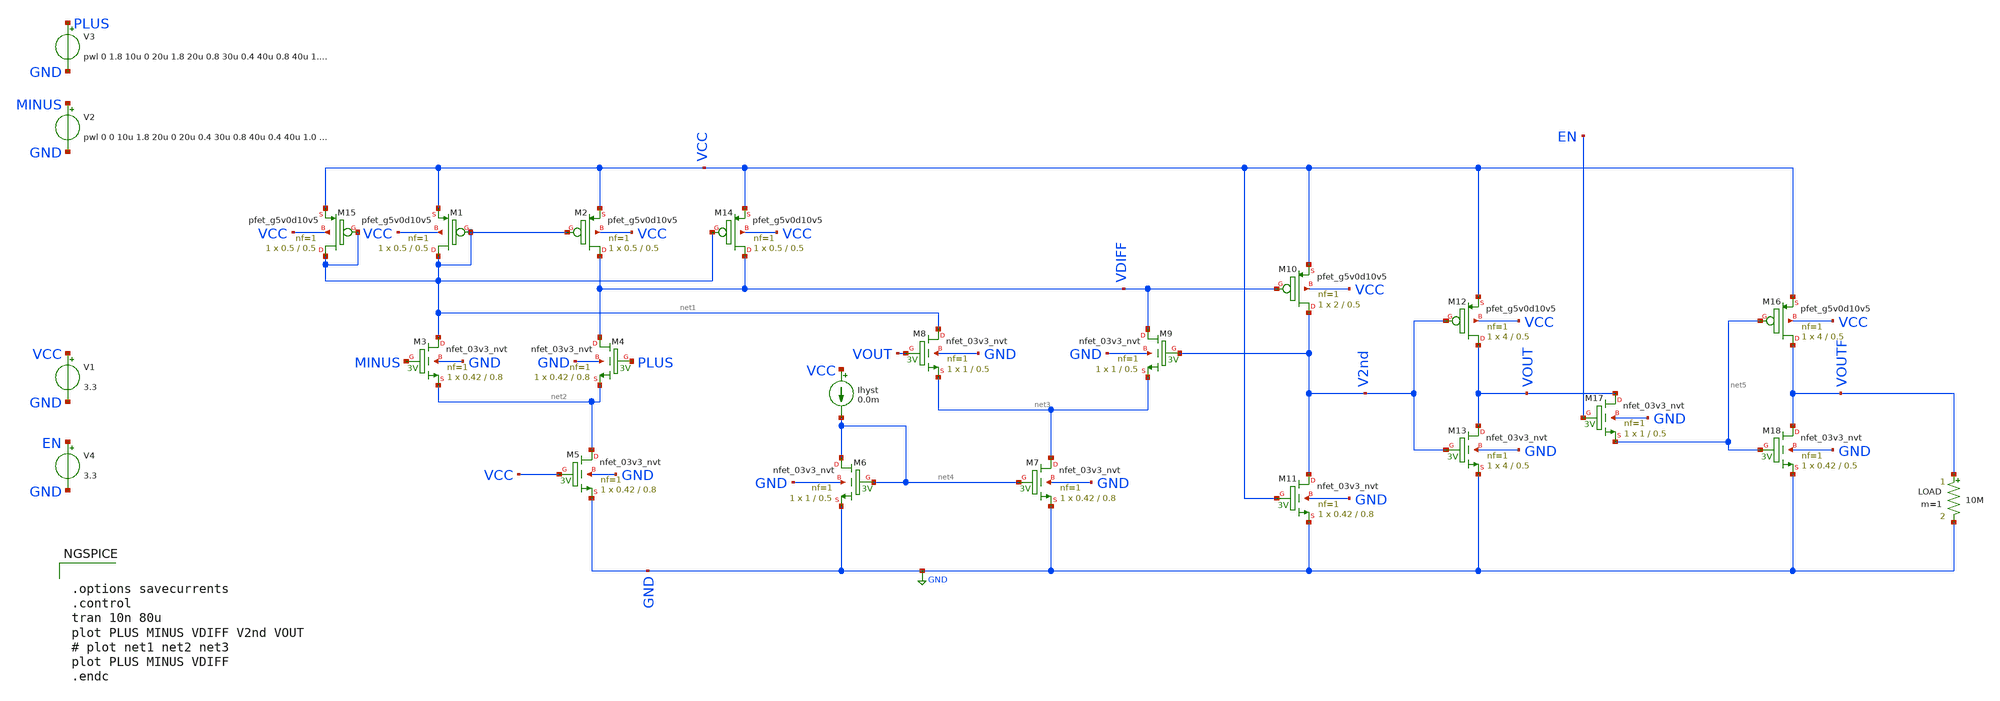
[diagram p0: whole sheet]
** sch_path: PreLayout/test_comparator.sch
* Copyright 2020 Stefan Frederik Schippers
* Licensed under the Apache License, Version 2.0 (the "License");
* you may not use this file except in compliance with the License.
* You may obtain a copy of the License at
* https://www.apache.org/licenses/LICENSE-2.0
* Unless required by applicable law or agreed to in writing, software
* distributed under the License is distributed on an "AS IS" BASIS,
* WITHOUT WARRANTIES OR CONDITIONS OF ANY KIND, either express or implied.
* See the License for the specific language governing permissions and
* limitations under the License.
**.subckt test_comparator
Ihyst VCC net4 0.0m
V1 VCC GND 3.3
V2 MINUS GND pwl 0 0 10u 1.8 20u 0 20u 0.4 30u 0.8 40u 0.4 40u 1.0 50u 1.4 60u 1.0 60u 2.2 70u 2.4
+ 80u 2.2
V3 PLUS GND pwl 0 1.8 10u 0 20u 1.8 20u 0.8 30u 0.4 40u 0.8 40u 1.4 50u 1.0 60u 1.4 60u 2.4 70u 2.2
+ 80u 2.4
XM3 net1 MINUS net2 GND sky130_fd_pr__nfet_03v3_nvt L=0.8 W=0.42 nf=1 ad='int((nf+1)/2) * W/nf * 0.29'
+ as='int((nf+2)/2) * W/nf * 0.29' pd='2*int((nf+1)/2) * (W/nf + 0.29)' ps='2*int((nf+2)/2) * (W/nf + 0.29)'
+ nrd='0.29 / W' nrs='0.29 / W' sa=0 sb=0 sd=0 mult=1 m=1
XM4 VDIFF PLUS net2 GND sky130_fd_pr__nfet_03v3_nvt L=0.8 W=0.42 nf=1 ad='int((nf+1)/2) * W/nf * 0.29'
+ as='int((nf+2)/2) * W/nf * 0.29' pd='2*int((nf+1)/2) * (W/nf + 0.29)' ps='2*int((nf+2)/2) * (W/nf + 0.29)'
+ nrd='0.29 / W' nrs='0.29 / W' sa=0 sb=0 sd=0 mult=1 m=1
XM8 net1 VOUT net3 GND sky130_fd_pr__nfet_03v3_nvt L=0.5 W=1 nf=1 ad='int((nf+1)/2) * W/nf * 0.29' as='int((nf+2)/2) * W/nf * 0.29'
+ pd='2*int((nf+1)/2) * (W/nf + 0.29)' ps='2*int((nf+2)/2) * (W/nf + 0.29)' nrd='0.29 / W' nrs='0.29 / W'
+ sa=0 sb=0 sd=0 mult=1 m=1
XM9 VDIFF V2nd net3 GND sky130_fd_pr__nfet_03v3_nvt L=0.5 W=1 nf=1 ad='int((nf+1)/2) * W/nf * 0.29' as='int((nf+2)/2) * W/nf * 0.29'
+ pd='2*int((nf+1)/2) * (W/nf + 0.29)' ps='2*int((nf+2)/2) * (W/nf + 0.29)' nrd='0.29 / W' nrs='0.29 / W'
+ sa=0 sb=0 sd=0 mult=1 m=1
XM5 net2 VCC GND GND sky130_fd_pr__nfet_03v3_nvt L=0.8 W=0.42 nf=1 ad='int((nf+1)/2) * W/nf * 0.29' as='int((nf+2)/2) * W/nf * 0.29'
+ pd='2*int((nf+1)/2) * (W/nf + 0.29)' ps='2*int((nf+2)/2) * (W/nf + 0.29)' nrd='0.29 / W' nrs='0.29 / W'
+ sa=0 sb=0 sd=0 mult=1 m=1
XM2 VDIFF net1 VCC VCC sky130_fd_pr__pfet_g5v0d10v5 L=0.5 W=0.5 nf=1 ad='int((nf+1)/2) * W/nf * 0.29'
+ as='int((nf+2)/2) * W/nf * 0.29' pd='2*int((nf+1)/2) * (W/nf + 0.29)' ps='2*int((nf+2)/2) * (W/nf + 0.29)'
+ nrd='0.29 / W' nrs='0.29 / W' sa=0 sb=0 sd=0 mult=1 m=1
XM1 net1 net1 VCC VCC sky130_fd_pr__pfet_g5v0d10v5 L=0.5 W=0.5 nf=1 ad='int((nf+1)/2) * W/nf * 0.29'
+ as='int((nf+2)/2) * W/nf * 0.29' pd='2*int((nf+1)/2) * (W/nf + 0.29)' ps='2*int((nf+2)/2) * (W/nf + 0.29)'
+ nrd='0.29 / W' nrs='0.29 / W' sa=0 sb=0 sd=0 mult=1 m=1
XM12 VOUT V2nd VCC VCC sky130_fd_pr__pfet_g5v0d10v5 L=0.5 W=4 nf=1 ad='int((nf+1)/2) * W/nf * 0.29' as='int((nf+2)/2) * W/nf * 0.29'
+ pd='2*int((nf+1)/2) * (W/nf + 0.29)' ps='2*int((nf+2)/2) * (W/nf + 0.29)' nrd='0.29 / W' nrs='0.29 / W'
+ sa=0 sb=0 sd=0 mult=1 m=1
XM10 V2nd VDIFF VCC VCC sky130_fd_pr__pfet_g5v0d10v5 L=0.5 W=2 nf=1 ad='int((nf+1)/2) * W/nf * 0.29'
+ as='int((nf+2)/2) * W/nf * 0.29' pd='2*int((nf+1)/2) * (W/nf + 0.29)' ps='2*int((nf+2)/2) * (W/nf + 0.29)'
+ nrd='0.29 / W' nrs='0.29 / W' sa=0 sb=0 sd=0 mult=1 m=1
XM13 VOUT V2nd GND GND sky130_fd_pr__nfet_03v3_nvt L=0.5 W=4 nf=1 ad='int((nf+1)/2) * W/nf * 0.29' as='int((nf+2)/2) * W/nf * 0.29'
+ pd='2*int((nf+1)/2) * (W/nf + 0.29)' ps='2*int((nf+2)/2) * (W/nf + 0.29)' nrd='0.29 / W' nrs='0.29 / W'
+ sa=0 sb=0 sd=0 mult=1 m=1
XM11 V2nd VCC GND GND sky130_fd_pr__nfet_03v3_nvt L=0.8 W=0.42 nf=1 ad='int((nf+1)/2) * W/nf * 0.29'
+ as='int((nf+2)/2) * W/nf * 0.29' pd='2*int((nf+1)/2) * (W/nf + 0.29)' ps='2*int((nf+2)/2) * (W/nf + 0.29)'
+ nrd='0.29 / W' nrs='0.29 / W' sa=0 sb=0 sd=0 mult=1 m=1
XM7 net3 net4 GND GND sky130_fd_pr__nfet_03v3_nvt L=0.8 W=0.42 nf=1 ad='int((nf+1)/2) * W/nf * 0.29'
+ as='int((nf+2)/2) * W/nf * 0.29' pd='2*int((nf+1)/2) * (W/nf + 0.29)' ps='2*int((nf+2)/2) * (W/nf + 0.29)'
+ nrd='0.29 / W' nrs='0.29 / W' sa=0 sb=0 sd=0 mult=1 m=1
XM6 net4 net4 GND GND sky130_fd_pr__nfet_03v3_nvt L=0.5 W=1 nf=1 ad='int((nf+1)/2) * W/nf * 0.29' as='int((nf+2)/2) * W/nf * 0.29'
+ pd='2*int((nf+1)/2) * (W/nf + 0.29)' ps='2*int((nf+2)/2) * (W/nf + 0.29)' nrd='0.29 / W' nrs='0.29 / W'
+ sa=0 sb=0 sd=0 mult=1 m=1
V4 EN GND 3.3
LOAD VOUTF GND 10M m=1
XM17 VOUT EN net5 GND sky130_fd_pr__nfet_03v3_nvt L=0.5 W=1 nf=1 ad='int((nf+1)/2) * W/nf * 0.29' as='int((nf+2)/2) * W/nf * 0.29'
+ pd='2*int((nf+1)/2) * (W/nf + 0.29)' ps='2*int((nf+2)/2) * (W/nf + 0.29)' nrd='0.29 / W' nrs='0.29 / W'
+ sa=0 sb=0 sd=0 mult=1 m=1
XM14 VDIFF net1 VCC VCC sky130_fd_pr__pfet_g5v0d10v5 L=0.5 W=0.5 nf=1 ad='int((nf+1)/2) * W/nf * 0.29'
+ as='int((nf+2)/2) * W/nf * 0.29' pd='2*int((nf+1)/2) * (W/nf + 0.29)' ps='2*int((nf+2)/2) * (W/nf + 0.29)'
+ nrd='0.29 / W' nrs='0.29 / W' sa=0 sb=0 sd=0 mult=1 m=1
XM15 net1 net1 VCC VCC sky130_fd_pr__pfet_g5v0d10v5 L=0.5 W=0.5 nf=1 ad='int((nf+1)/2) * W/nf * 0.29'
+ as='int((nf+2)/2) * W/nf * 0.29' pd='2*int((nf+1)/2) * (W/nf + 0.29)' ps='2*int((nf+2)/2) * (W/nf + 0.29)'
+ nrd='0.29 / W' nrs='0.29 / W' sa=0 sb=0 sd=0 mult=1 m=1
XM16 VOUTF net5 VCC VCC sky130_fd_pr__pfet_g5v0d10v5 L=0.5 W=4 nf=1 ad='int((nf+1)/2) * W/nf * 0.29'
+ as='int((nf+2)/2) * W/nf * 0.29' pd='2*int((nf+1)/2) * (W/nf + 0.29)' ps='2*int((nf+2)/2) * (W/nf + 0.29)'
+ nrd='0.29 / W' nrs='0.29 / W' sa=0 sb=0 sd=0 mult=1 m=1
XM18 VOUTF net5 GND GND sky130_fd_pr__nfet_03v3_nvt L=0.5 W=0.42 nf=1 ad='int((nf+1)/2) * W/nf * 0.29'
+ as='int((nf+2)/2) * W/nf * 0.29' pd='2*int((nf+1)/2) * (W/nf + 0.29)' ps='2*int((nf+2)/2) * (W/nf + 0.29)'
+ nrd='0.29 / W' nrs='0.29 / W' sa=0 sb=0 sd=0 mult=1 m=1
**** begin user architecture code

.include $::SKYWATER_MODELS/cells/nfet_01v8/sky130_fd_pr__nfet_01v8__tt.corner.spice
.include $::SKYWATER_MODELS/cells/nfet_01v8_lvt/sky130_fd_pr__nfet_01v8_lvt__tt.corner.spice
.include $::SKYWATER_MODELS/cells/pfet_01v8/sky130_fd_pr__pfet_01v8__tt.corner.spice
.include $::SKYWATER_MODELS/cells/nfet_03v3_nvt/sky130_fd_pr__nfet_03v3_nvt__tt.corner.spice
.include $::SKYWATER_MODELS/cells/nfet_05v0_nvt/sky130_fd_pr__nfet_05v0_nvt__tt.corner.spice
.include $::SKYWATER_MODELS/cells/esd_nfet_01v8/sky130_fd_pr__esd_nfet_01v8__tt.corner.spice
.include $::SKYWATER_MODELS/cells/pfet_01v8_lvt/sky130_fd_pr__pfet_01v8_lvt__tt.corner.spice
.include $::SKYWATER_MODELS/cells/pfet_01v8_hvt/sky130_fd_pr__pfet_01v8_hvt__tt.corner.spice
.include $::SKYWATER_MODELS/cells/esd_pfet_g5v0d10v5/sky130_fd_pr__esd_pfet_g5v0d10v5__tt.corner.spice
.include $::SKYWATER_MODELS/cells/pfet_g5v0d10v5/sky130_fd_pr__pfet_g5v0d10v5__tt.corner.spice
.include $::SKYWATER_MODELS/cells/pfet_g5v0d16v0/sky130_fd_pr__pfet_g5v0d16v0__tt.corner.spice
.include $::SKYWATER_MODELS/cells/nfet_g5v0d10v5/sky130_fd_pr__nfet_g5v0d10v5__tt.corner.spice
.include $::SKYWATER_MODELS/cells/nfet_g5v0d16v0/sky130_fd_pr__nfet_g5v0d16v0__tt_discrete.corner.spice
.include $::SKYWATER_MODELS/cells/esd_nfet_g5v0d10v5/sky130_fd_pr__esd_nfet_g5v0d10v5__tt.corner.spice
.include $::SKYWATER_MODELS/models/corners/tt/nonfet.spice
* Mismatch parameters
.include $::SKYWATER_MODELS/cells/nfet_01v8/sky130_fd_pr__nfet_01v8__mismatch.corner.spice
.include $::SKYWATER_MODELS/cells/pfet_01v8/sky130_fd_pr__pfet_01v8__mismatch.corner.spice
.include $::SKYWATER_MODELS/cells/nfet_01v8_lvt/sky130_fd_pr__nfet_01v8_lvt__mismatch.corner.spice
.include $::SKYWATER_MODELS/cells/pfet_01v8_lvt/sky130_fd_pr__pfet_01v8_lvt__mismatch.corner.spice
.include $::SKYWATER_MODELS/cells/pfet_01v8_hvt/sky130_fd_pr__pfet_01v8_hvt__mismatch.corner.spice
.include $::SKYWATER_MODELS/cells/nfet_g5v0d10v5/sky130_fd_pr__nfet_g5v0d10v5__mismatch.corner.spice
.include $::SKYWATER_MODELS/cells/pfet_g5v0d10v5/sky130_fd_pr__pfet_g5v0d10v5__mismatch.corner.spice
.include $::SKYWATER_MODELS/cells/nfet_05v0_nvt/sky130_fd_pr__nfet_05v0_nvt__mismatch.corner.spice
.include $::SKYWATER_MODELS/cells/nfet_03v3_nvt/sky130_fd_pr__nfet_03v3_nvt__mismatch.corner.spice
* Resistor$::SKYWATER_MODELS/Capacitor
.include $::SKYWATER_MODELS/models/r+c/res_typical__cap_typical.spice
.include $::SKYWATER_MODELS/models/r+c/res_typical__cap_typical__lin.spice
* Special cells
.include $::SKYWATER_MODELS/models/corners/tt/specialized_cells.spice
* All models
.include $::SKYWATER_MODELS/models/all.spice
* Corner
.include $::SKYWATER_MODELS/models/corners/tt/rf.spice



.options savecurrents
.control
tran 10n 80u
plot PLUS MINUS VDIFF V2nd VOUT
# plot net1 net2 net3
plot PLUS MINUS VDIFF
.endc


**** end user architecture code
**.ends
.GLOBAL GND
.end
